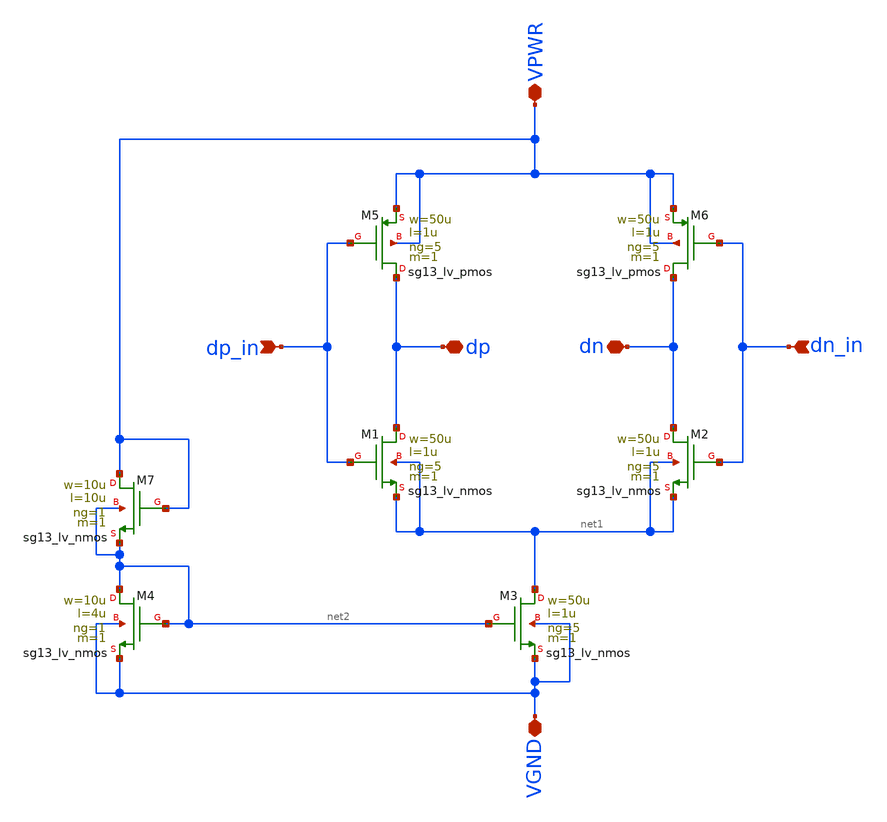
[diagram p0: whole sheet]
** sch_path: xschem/lvds.sch
**.subckt lvds dp_in dn_in VPWR VGND dp dn
*.ipin dp_in
*.ipin dn_in
*.iopin VPWR
*.iopin VGND
*.iopin dp
*.iopin dn
XM1 dp dp_in net1 net1 sg13_lv_nmos w=50u l=1u ng=5 m=1 mm_ok=1
XM2 dn dn_in net1 net1 sg13_lv_nmos w=50u l=1u ng=5 m=1 mm_ok=1
XM5 dp dp_in VPWR VPWR sg13_lv_pmos w=50u l=1u ng=5 m=1 mm_ok=1
XM6 dn dn_in VPWR VPWR sg13_lv_pmos w=50u l=1u ng=5 m=1 mm_ok=1
XM3 net1 net2 VGND VGND sg13_lv_nmos w=50u l=1u ng=5 m=1 mm_ok=1
XM4 net2 net2 VGND VGND sg13_lv_nmos w=10u l=4u ng=1 m=1 mm_ok=1
XM7 VPWR VPWR net2 net2 sg13_lv_nmos w=10u l=10u ng=1 m=1 mm_ok=1
**.ends
.end
